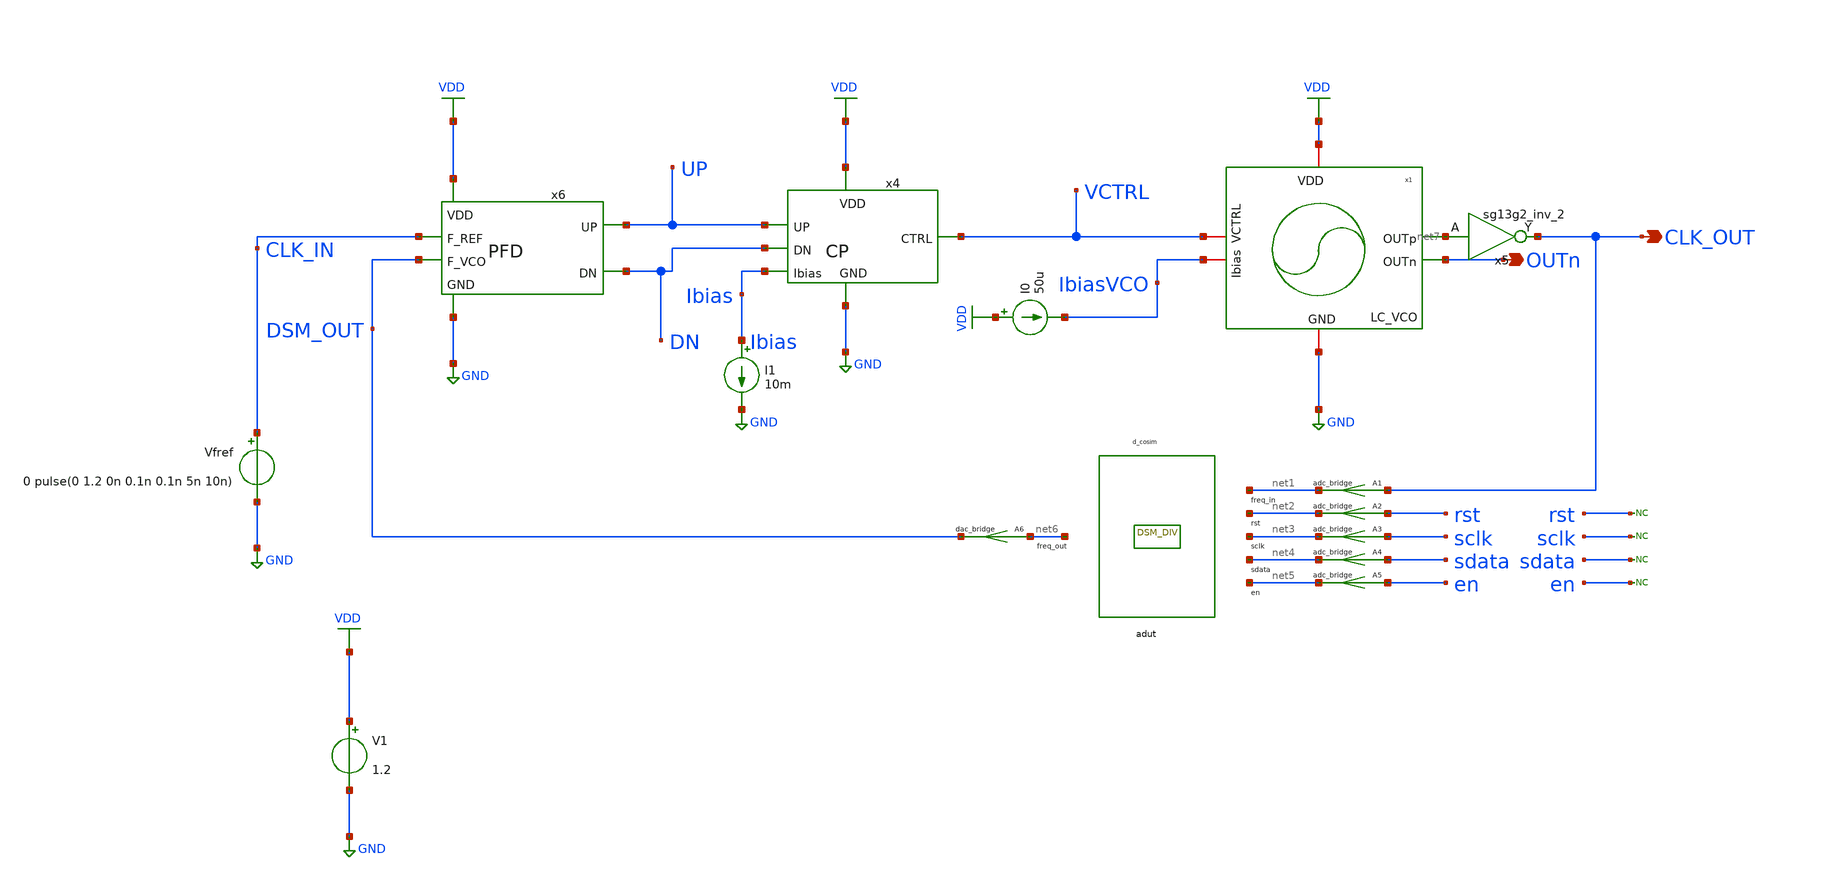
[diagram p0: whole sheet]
** sch_path: xschem/Test/pll_dsm_freqdivider_tb.sch
**.subckt pll_dsm_freqdivider_tb OUTn CLK_OUT
*.opin OUTn
*.opin CLK_OUT
V1 VDD GND 1.2
I0 VDD IbiasVCO 50u
Vfref CLK_IN GND 0 pulse(0 1.2 0n 0.1n 0.1n 5n 10n)
I1 Ibias GND 10m
x5 CLK_OUT net7 VDD GND sg13g2_inv_2
* noconn rst
* noconn sclk
* noconn sdata
* noconn en
x4 VDD UP VCTRL DN GND Ibias CP
x6 VDD UP CLK_IN DSM_OUT DN GND PFD
adut [ net1 net2 net3 net4 net5 ] [ net6 ] null dut
.model dut d_cosim simulation=./../dsm_and_freq_divider.so
A1 [ CLK_OUT ] [ net1 ] adc1
.model adc1 adc_bridge in_low=0.4 in_high=0.6
A2 [ rst ] [ net2 ] adc1
.model adc1 adc_bridge in_low=0.4 in_high=0.6
A3 [ sclk ] [ net3 ] adc1
.model adc1 adc_bridge in_low=0.4 in_high=0.6
A4 [ sdata ] [ net4 ] adc1
.model adc1 adc_bridge in_low=0.4 in_high=0.6
A5 [ en ] [ net5 ] adc1
.model adc1 adc_bridge in_low=0.4 in_high=0.6
A6 [ net6 ] [ DSM_OUT ] dac1
.model dac1 dac_bridge out_low=0 out_high=1.2
x1 VDD net7 OUTn IbiasVCO VCTRL GND LC_VCO
**** begin user architecture code



*****************************************************
* PLL + DSM Frequency Divider Testbench
*****************************************************

.option temp = 27
.param VDD = 1.2

* ==============================
* Include Models
* ==============================

* Inductor / analog models
.include ./IHP_4nH_Inductor.spice

.control
  save v(sdata) v(sclk) v(rst) v(en) v(UP) v(DN) v(VCTRL) v(CLK_IN) v(DSM_OUT) v(CLK_OUT)
  * Simulation accuracy options
  .options maxstep=10p reltol=1e-4 abstol=1e-9

 * Run long enough for PLL lock
  tran 20p 5u uic
  remzerovec
  write pll_dsm_div.raw
.endc
* to generate following file copy stimuli.test
* to the simulation directory and run simulation -> Utile Stimuli Editor (GUI),
* and press 'Translate'
.include stimuli_test.cir






.lib cornerMOSlv.lib mos_tt
.lib cornerHBT.lib hbt_typ
.lib cornerRES.lib res_typ
.lib cornerCAP.lib cap_typ_stat
.include /foss/pdks/ihp-sg13g2/libs.ref/sg13g2_stdcell/spice/sg13g2_stdcell.spice
.global VDD GND


.param CP_N_L = 0.5u
.param CP_N_W = 10u
.param CP_P_M = 1
.param CP_P_L = 0.5u
.param CP_P_W = 30u
.param CP_N_M = 1
.param C_CP = 400p



**** end user architecture code
**.ends
.GLOBAL GND
.GLOBAL VDD
.end
